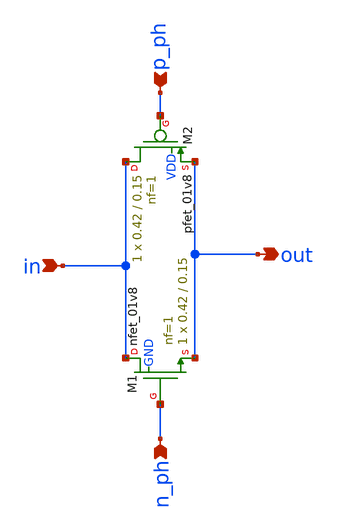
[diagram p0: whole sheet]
** sch_path: tutorial_5/tgate.sch
**.subckt tgate in out p_ph n_ph
*.ipin in
*.opin out
*.ipin p_ph
*.ipin n_ph
XM1 in n_ph out GND sky130_fd_pr__nfet_01v8 L=0.15 W=0.42 nf=1 ad='int((nf+1)/2) * W/nf * 0.29' as='int((nf+2)/2) * W/nf * 0.29'
+ pd='2*int((nf+1)/2) * (W/nf + 0.29)' ps='2*int((nf+2)/2) * (W/nf + 0.29)' nrd='0.29 / W' nrs='0.29 / W'
+ sa=0 sb=0 sd=0 mult=1 m=1
XM2 in p_ph out VDD sky130_fd_pr__pfet_01v8 L=0.15 W=0.42 nf=1 ad='int((nf+1)/2) * W/nf * 0.29' as='int((nf+2)/2) * W/nf * 0.29'
+ pd='2*int((nf+1)/2) * (W/nf + 0.29)' ps='2*int((nf+2)/2) * (W/nf + 0.29)' nrd='0.29 / W' nrs='0.29 / W'
+ sa=0 sb=0 sd=0 mult=1 m=1
**.ends
.end
